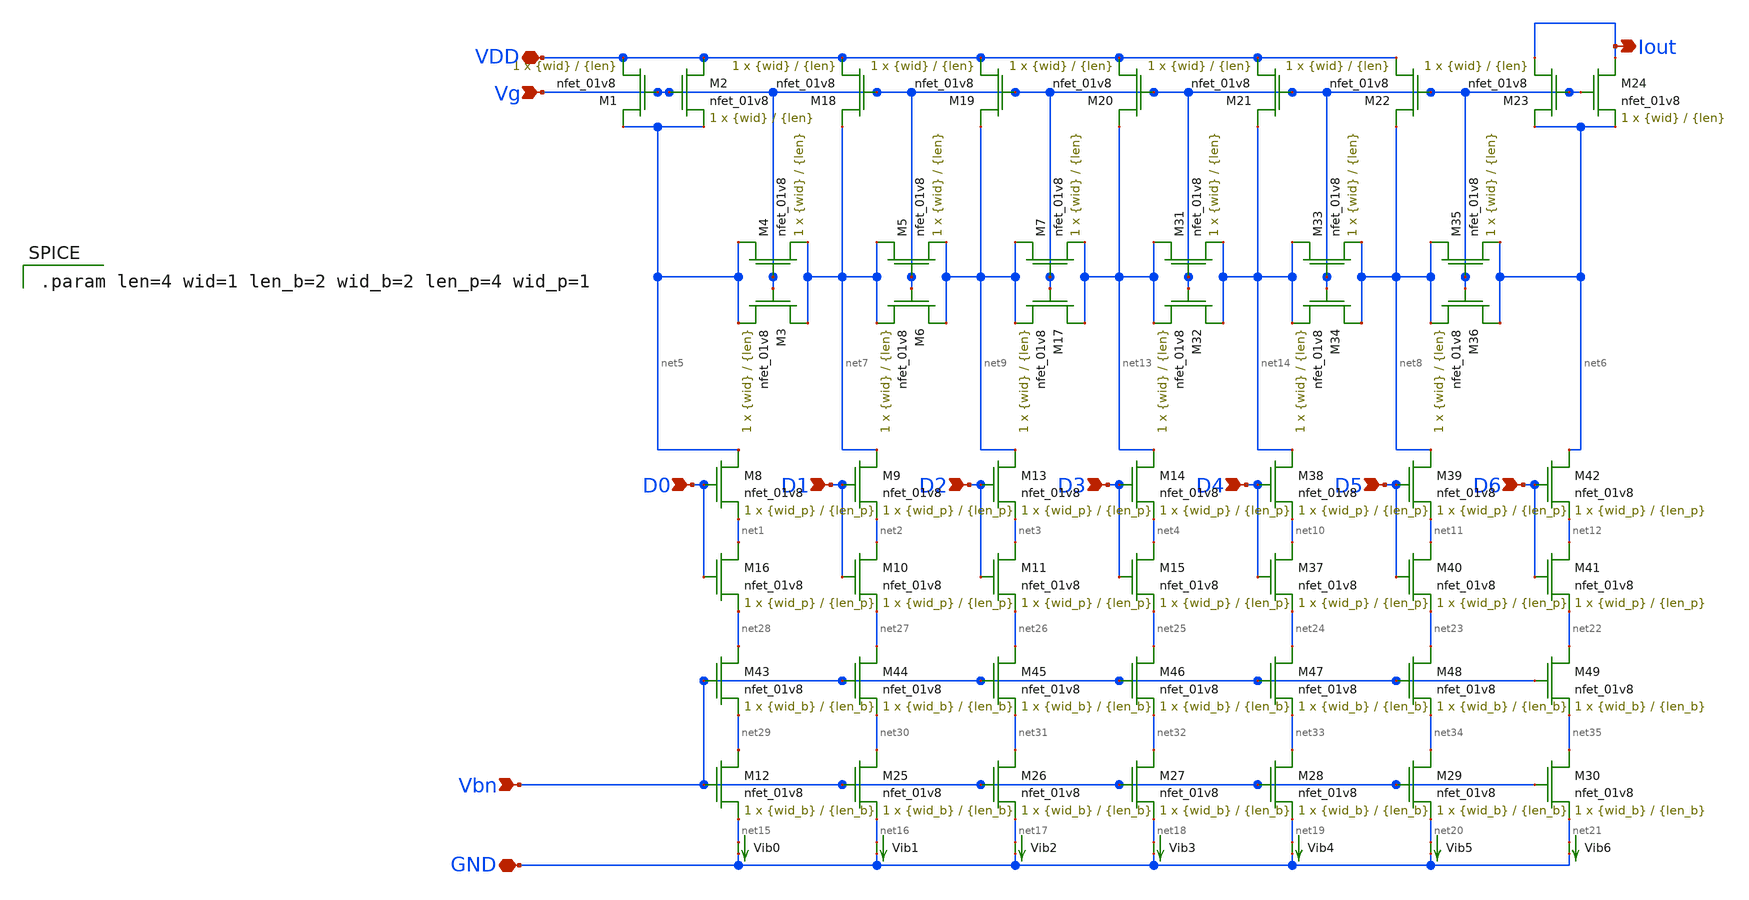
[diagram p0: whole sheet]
** sch_path: mp3/ladder.sch
**.subckt ladder Vbn VDD Iout GND D0 D1 D2 D3 D4 D5 D6 Vg
*.ipin Vbn
*.iopin VDD
*.opin Iout
*.iopin GND
*.ipin D0
*.ipin D1
*.ipin D2
*.ipin D3
*.ipin D4
*.ipin D5
*.ipin D6
*.ipin Vg
XM1 net5 Vg VDD GND sky130_fd_pr__nfet_01v8 L={len} W={wid} nf=1 ad='int((nf+1)/2) * W/nf * 0.29' as='int((nf+2)/2) * W/nf * 0.29'
+ pd='2*int((nf+1)/2) * (W/nf + 0.29)' ps='2*int((nf+2)/2) * (W/nf + 0.29)' nrd='0.29 / W' nrs='0.29 / W'
+ sa=0 sb=0 sd=0 mult=1 m=1
XM4 net5 Vg net7 GND sky130_fd_pr__nfet_01v8 L={len} W={wid} nf=1 ad='int((nf+1)/2) * W/nf * 0.29' as='int((nf+2)/2) * W/nf * 0.29'
+ pd='2*int((nf+1)/2) * (W/nf + 0.29)' ps='2*int((nf+2)/2) * (W/nf + 0.29)' nrd='0.29 / W' nrs='0.29 / W'
+ sa=0 sb=0 sd=0 mult=1 m=1
XM12 net29 Vbn net15 GND sky130_fd_pr__nfet_01v8 L={len_b} W={wid_b} nf=1 ad='int((nf+1)/2) * W/nf * 0.29'
+ as='int((nf+2)/2) * W/nf * 0.29' pd='2*int((nf+1)/2) * (W/nf + 0.29)' ps='2*int((nf+2)/2) * (W/nf + 0.29)'
+ nrd='0.29 / W' nrs='0.29 / W' sa=0 sb=0 sd=0 mult=1 m=1
XM2 VDD Vg net5 GND sky130_fd_pr__nfet_01v8 L={len} W={wid} nf=1 ad='int((nf+1)/2) * W/nf * 0.29' as='int((nf+2)/2) * W/nf * 0.29'
+ pd='2*int((nf+1)/2) * (W/nf + 0.29)' ps='2*int((nf+2)/2) * (W/nf + 0.29)' nrd='0.29 / W' nrs='0.29 / W'
+ sa=0 sb=0 sd=0 mult=1 m=1
XM18 net7 Vg VDD GND sky130_fd_pr__nfet_01v8 L={len} W={wid} nf=1 ad='int((nf+1)/2) * W/nf * 0.29' as='int((nf+2)/2) * W/nf * 0.29'
+ pd='2*int((nf+1)/2) * (W/nf + 0.29)' ps='2*int((nf+2)/2) * (W/nf + 0.29)' nrd='0.29 / W' nrs='0.29 / W'
+ sa=0 sb=0 sd=0 mult=1 m=1
XM19 net9 Vg VDD GND sky130_fd_pr__nfet_01v8 L={len} W={wid} nf=1 ad='int((nf+1)/2) * W/nf * 0.29' as='int((nf+2)/2) * W/nf * 0.29'
+ pd='2*int((nf+1)/2) * (W/nf + 0.29)' ps='2*int((nf+2)/2) * (W/nf + 0.29)' nrd='0.29 / W' nrs='0.29 / W'
+ sa=0 sb=0 sd=0 mult=1 m=1
XM20 net13 Vg VDD GND sky130_fd_pr__nfet_01v8 L={len} W={wid} nf=1 ad='int((nf+1)/2) * W/nf * 0.29' as='int((nf+2)/2) * W/nf * 0.29'
+ pd='2*int((nf+1)/2) * (W/nf + 0.29)' ps='2*int((nf+2)/2) * (W/nf + 0.29)' nrd='0.29 / W' nrs='0.29 / W'
+ sa=0 sb=0 sd=0 mult=1 m=1
XM21 net14 Vg VDD GND sky130_fd_pr__nfet_01v8 L={len} W={wid} nf=1 ad='int((nf+1)/2) * W/nf * 0.29' as='int((nf+2)/2) * W/nf * 0.29'
+ pd='2*int((nf+1)/2) * (W/nf + 0.29)' ps='2*int((nf+2)/2) * (W/nf + 0.29)' nrd='0.29 / W' nrs='0.29 / W'
+ sa=0 sb=0 sd=0 mult=1 m=1
XM22 net8 Vg VDD GND sky130_fd_pr__nfet_01v8 L={len} W={wid} nf=1 ad='int((nf+1)/2) * W/nf * 0.29' as='int((nf+2)/2) * W/nf * 0.29'
+ pd='2*int((nf+1)/2) * (W/nf + 0.29)' ps='2*int((nf+2)/2) * (W/nf + 0.29)' nrd='0.29 / W' nrs='0.29 / W'
+ sa=0 sb=0 sd=0 mult=1 m=1
XM23 net6 Vg Iout GND sky130_fd_pr__nfet_01v8 L={len} W={wid} nf=1 ad='int((nf+1)/2) * W/nf * 0.29' as='int((nf+2)/2) * W/nf * 0.29'
+ pd='2*int((nf+1)/2) * (W/nf + 0.29)' ps='2*int((nf+2)/2) * (W/nf + 0.29)' nrd='0.29 / W' nrs='0.29 / W'
+ sa=0 sb=0 sd=0 mult=1 m=1
XM24 Iout Vg net6 GND sky130_fd_pr__nfet_01v8 L={len} W={wid} nf=1 ad='int((nf+1)/2) * W/nf * 0.29' as='int((nf+2)/2) * W/nf * 0.29'
+ pd='2*int((nf+1)/2) * (W/nf + 0.29)' ps='2*int((nf+2)/2) * (W/nf + 0.29)' nrd='0.29 / W' nrs='0.29 / W'
+ sa=0 sb=0 sd=0 mult=1 m=1
XM3 net7 Vg net5 GND sky130_fd_pr__nfet_01v8 L={len} W={wid} nf=1 ad='int((nf+1)/2) * W/nf * 0.29' as='int((nf+2)/2) * W/nf * 0.29'
+ pd='2*int((nf+1)/2) * (W/nf + 0.29)' ps='2*int((nf+2)/2) * (W/nf + 0.29)' nrd='0.29 / W' nrs='0.29 / W'
+ sa=0 sb=0 sd=0 mult=1 m=1
XM5 net7 Vg net9 GND sky130_fd_pr__nfet_01v8 L={len} W={wid} nf=1 ad='int((nf+1)/2) * W/nf * 0.29' as='int((nf+2)/2) * W/nf * 0.29'
+ pd='2*int((nf+1)/2) * (W/nf + 0.29)' ps='2*int((nf+2)/2) * (W/nf + 0.29)' nrd='0.29 / W' nrs='0.29 / W'
+ sa=0 sb=0 sd=0 mult=1 m=1
XM6 net9 Vg net7 GND sky130_fd_pr__nfet_01v8 L={len} W={wid} nf=1 ad='int((nf+1)/2) * W/nf * 0.29' as='int((nf+2)/2) * W/nf * 0.29'
+ pd='2*int((nf+1)/2) * (W/nf + 0.29)' ps='2*int((nf+2)/2) * (W/nf + 0.29)' nrd='0.29 / W' nrs='0.29 / W'
+ sa=0 sb=0 sd=0 mult=1 m=1
XM7 net9 Vg net13 GND sky130_fd_pr__nfet_01v8 L={len} W={wid} nf=1 ad='int((nf+1)/2) * W/nf * 0.29' as='int((nf+2)/2) * W/nf * 0.29'
+ pd='2*int((nf+1)/2) * (W/nf + 0.29)' ps='2*int((nf+2)/2) * (W/nf + 0.29)' nrd='0.29 / W' nrs='0.29 / W'
+ sa=0 sb=0 sd=0 mult=1 m=1
XM17 net13 Vg net9 GND sky130_fd_pr__nfet_01v8 L={len} W={wid} nf=1 ad='int((nf+1)/2) * W/nf * 0.29'
+ as='int((nf+2)/2) * W/nf * 0.29' pd='2*int((nf+1)/2) * (W/nf + 0.29)' ps='2*int((nf+2)/2) * (W/nf + 0.29)'
+ nrd='0.29 / W' nrs='0.29 / W' sa=0 sb=0 sd=0 mult=1 m=1
XM31 net13 Vg net14 GND sky130_fd_pr__nfet_01v8 L={len} W={wid} nf=1 ad='int((nf+1)/2) * W/nf * 0.29'
+ as='int((nf+2)/2) * W/nf * 0.29' pd='2*int((nf+1)/2) * (W/nf + 0.29)' ps='2*int((nf+2)/2) * (W/nf + 0.29)'
+ nrd='0.29 / W' nrs='0.29 / W' sa=0 sb=0 sd=0 mult=1 m=1
XM32 net14 Vg net13 GND sky130_fd_pr__nfet_01v8 L={len} W={wid} nf=1 ad='int((nf+1)/2) * W/nf * 0.29'
+ as='int((nf+2)/2) * W/nf * 0.29' pd='2*int((nf+1)/2) * (W/nf + 0.29)' ps='2*int((nf+2)/2) * (W/nf + 0.29)'
+ nrd='0.29 / W' nrs='0.29 / W' sa=0 sb=0 sd=0 mult=1 m=1
XM33 net14 Vg net8 GND sky130_fd_pr__nfet_01v8 L={len} W={wid} nf=1 ad='int((nf+1)/2) * W/nf * 0.29'
+ as='int((nf+2)/2) * W/nf * 0.29' pd='2*int((nf+1)/2) * (W/nf + 0.29)' ps='2*int((nf+2)/2) * (W/nf + 0.29)'
+ nrd='0.29 / W' nrs='0.29 / W' sa=0 sb=0 sd=0 mult=1 m=1
XM34 net8 Vg net14 GND sky130_fd_pr__nfet_01v8 L={len} W={wid} nf=1 ad='int((nf+1)/2) * W/nf * 0.29'
+ as='int((nf+2)/2) * W/nf * 0.29' pd='2*int((nf+1)/2) * (W/nf + 0.29)' ps='2*int((nf+2)/2) * (W/nf + 0.29)'
+ nrd='0.29 / W' nrs='0.29 / W' sa=0 sb=0 sd=0 mult=1 m=1
XM35 net8 Vg net6 GND sky130_fd_pr__nfet_01v8 L={len} W={wid} nf=1 ad='int((nf+1)/2) * W/nf * 0.29' as='int((nf+2)/2) * W/nf * 0.29'
+ pd='2*int((nf+1)/2) * (W/nf + 0.29)' ps='2*int((nf+2)/2) * (W/nf + 0.29)' nrd='0.29 / W' nrs='0.29 / W'
+ sa=0 sb=0 sd=0 mult=1 m=1
XM36 net6 Vg net8 GND sky130_fd_pr__nfet_01v8 L={len} W={wid} nf=1 ad='int((nf+1)/2) * W/nf * 0.29' as='int((nf+2)/2) * W/nf * 0.29'
+ pd='2*int((nf+1)/2) * (W/nf + 0.29)' ps='2*int((nf+2)/2) * (W/nf + 0.29)' nrd='0.29 / W' nrs='0.29 / W'
+ sa=0 sb=0 sd=0 mult=1 m=1
Vib0 net15 GND 0
.save i(vib0)
Vib1 net16 GND 0
.save i(vib1)
Vib2 net17 GND 0
.save i(vib2)
Vib3 net18 GND 0
.save i(vib3)
Vib4 net19 GND 0
.save i(vib4)
Vib5 net20 GND 0
.save i(vib5)
Vib6 net21 GND 0
.save i(vib6)
XM16 net1 D0 net28 GND sky130_fd_pr__nfet_01v8 L={len_p} W={wid_p} nf=1 ad='int((nf+1)/2) * W/nf * 0.29'
+ as='int((nf+2)/2) * W/nf * 0.29' pd='2*int((nf+1)/2) * (W/nf + 0.29)' ps='2*int((nf+2)/2) * (W/nf + 0.29)'
+ nrd='0.29 / W' nrs='0.29 / W' sa=0 sb=0 sd=0 mult=1 m=1
XM8 net5 D0 net1 GND sky130_fd_pr__nfet_01v8 L={len_p} W={wid_p} nf=1 ad='int((nf+1)/2) * W/nf * 0.29'
+ as='int((nf+2)/2) * W/nf * 0.29' pd='2*int((nf+1)/2) * (W/nf + 0.29)' ps='2*int((nf+2)/2) * (W/nf + 0.29)'
+ nrd='0.29 / W' nrs='0.29 / W' sa=0 sb=0 sd=0 mult=1 m=1
XM9 net7 D1 net2 GND sky130_fd_pr__nfet_01v8 L={len_p} W={wid_p} nf=1 ad='int((nf+1)/2) * W/nf * 0.29'
+ as='int((nf+2)/2) * W/nf * 0.29' pd='2*int((nf+1)/2) * (W/nf + 0.29)' ps='2*int((nf+2)/2) * (W/nf + 0.29)'
+ nrd='0.29 / W' nrs='0.29 / W' sa=0 sb=0 sd=0 mult=1 m=1
XM10 net2 D1 net27 GND sky130_fd_pr__nfet_01v8 L={len_p} W={wid_p} nf=1 ad='int((nf+1)/2) * W/nf * 0.29'
+ as='int((nf+2)/2) * W/nf * 0.29' pd='2*int((nf+1)/2) * (W/nf + 0.29)' ps='2*int((nf+2)/2) * (W/nf + 0.29)'
+ nrd='0.29 / W' nrs='0.29 / W' sa=0 sb=0 sd=0 mult=1 m=1
XM11 net3 D2 net26 GND sky130_fd_pr__nfet_01v8 L={len_p} W={wid_p} nf=1 ad='int((nf+1)/2) * W/nf * 0.29'
+ as='int((nf+2)/2) * W/nf * 0.29' pd='2*int((nf+1)/2) * (W/nf + 0.29)' ps='2*int((nf+2)/2) * (W/nf + 0.29)'
+ nrd='0.29 / W' nrs='0.29 / W' sa=0 sb=0 sd=0 mult=1 m=1
XM13 net9 D2 net3 GND sky130_fd_pr__nfet_01v8 L={len_p} W={wid_p} nf=1 ad='int((nf+1)/2) * W/nf * 0.29'
+ as='int((nf+2)/2) * W/nf * 0.29' pd='2*int((nf+1)/2) * (W/nf + 0.29)' ps='2*int((nf+2)/2) * (W/nf + 0.29)'
+ nrd='0.29 / W' nrs='0.29 / W' sa=0 sb=0 sd=0 mult=1 m=1
XM14 net13 D3 net4 GND sky130_fd_pr__nfet_01v8 L={len_p} W={wid_p} nf=1 ad='int((nf+1)/2) * W/nf * 0.29'
+ as='int((nf+2)/2) * W/nf * 0.29' pd='2*int((nf+1)/2) * (W/nf + 0.29)' ps='2*int((nf+2)/2) * (W/nf + 0.29)'
+ nrd='0.29 / W' nrs='0.29 / W' sa=0 sb=0 sd=0 mult=1 m=1
XM15 net4 D3 net25 GND sky130_fd_pr__nfet_01v8 L={len_p} W={wid_p} nf=1 ad='int((nf+1)/2) * W/nf * 0.29'
+ as='int((nf+2)/2) * W/nf * 0.29' pd='2*int((nf+1)/2) * (W/nf + 0.29)' ps='2*int((nf+2)/2) * (W/nf + 0.29)'
+ nrd='0.29 / W' nrs='0.29 / W' sa=0 sb=0 sd=0 mult=1 m=1
XM37 net10 D4 net24 GND sky130_fd_pr__nfet_01v8 L={len_p} W={wid_p} nf=1 ad='int((nf+1)/2) * W/nf * 0.29'
+ as='int((nf+2)/2) * W/nf * 0.29' pd='2*int((nf+1)/2) * (W/nf + 0.29)' ps='2*int((nf+2)/2) * (W/nf + 0.29)'
+ nrd='0.29 / W' nrs='0.29 / W' sa=0 sb=0 sd=0 mult=1 m=1
XM38 net14 D4 net10 GND sky130_fd_pr__nfet_01v8 L={len_p} W={wid_p} nf=1 ad='int((nf+1)/2) * W/nf * 0.29'
+ as='int((nf+2)/2) * W/nf * 0.29' pd='2*int((nf+1)/2) * (W/nf + 0.29)' ps='2*int((nf+2)/2) * (W/nf + 0.29)'
+ nrd='0.29 / W' nrs='0.29 / W' sa=0 sb=0 sd=0 mult=1 m=1
XM39 net8 D5 net11 GND sky130_fd_pr__nfet_01v8 L={len_p} W={wid_p} nf=1 ad='int((nf+1)/2) * W/nf * 0.29'
+ as='int((nf+2)/2) * W/nf * 0.29' pd='2*int((nf+1)/2) * (W/nf + 0.29)' ps='2*int((nf+2)/2) * (W/nf + 0.29)'
+ nrd='0.29 / W' nrs='0.29 / W' sa=0 sb=0 sd=0 mult=1 m=1
XM40 net11 D5 net23 GND sky130_fd_pr__nfet_01v8 L={len_p} W={wid_p} nf=1 ad='int((nf+1)/2) * W/nf * 0.29'
+ as='int((nf+2)/2) * W/nf * 0.29' pd='2*int((nf+1)/2) * (W/nf + 0.29)' ps='2*int((nf+2)/2) * (W/nf + 0.29)'
+ nrd='0.29 / W' nrs='0.29 / W' sa=0 sb=0 sd=0 mult=1 m=1
XM41 net12 D6 net22 GND sky130_fd_pr__nfet_01v8 L={len_p} W={wid_p} nf=1 ad='int((nf+1)/2) * W/nf * 0.29'
+ as='int((nf+2)/2) * W/nf * 0.29' pd='2*int((nf+1)/2) * (W/nf + 0.29)' ps='2*int((nf+2)/2) * (W/nf + 0.29)'
+ nrd='0.29 / W' nrs='0.29 / W' sa=0 sb=0 sd=0 mult=1 m=1
XM42 net6 D6 net12 GND sky130_fd_pr__nfet_01v8 L={len_p} W={wid_p} nf=1 ad='int((nf+1)/2) * W/nf * 0.29'
+ as='int((nf+2)/2) * W/nf * 0.29' pd='2*int((nf+1)/2) * (W/nf + 0.29)' ps='2*int((nf+2)/2) * (W/nf + 0.29)'
+ nrd='0.29 / W' nrs='0.29 / W' sa=0 sb=0 sd=0 mult=1 m=1
XM25 net30 Vbn net16 GND sky130_fd_pr__nfet_01v8 L={len_b} W={wid_b} nf=1 ad='int((nf+1)/2) * W/nf * 0.29'
+ as='int((nf+2)/2) * W/nf * 0.29' pd='2*int((nf+1)/2) * (W/nf + 0.29)' ps='2*int((nf+2)/2) * (W/nf + 0.29)'
+ nrd='0.29 / W' nrs='0.29 / W' sa=0 sb=0 sd=0 mult=1 m=1
XM26 net31 Vbn net17 GND sky130_fd_pr__nfet_01v8 L={len_b} W={wid_b} nf=1 ad='int((nf+1)/2) * W/nf * 0.29'
+ as='int((nf+2)/2) * W/nf * 0.29' pd='2*int((nf+1)/2) * (W/nf + 0.29)' ps='2*int((nf+2)/2) * (W/nf + 0.29)'
+ nrd='0.29 / W' nrs='0.29 / W' sa=0 sb=0 sd=0 mult=1 m=1
XM27 net32 Vbn net18 GND sky130_fd_pr__nfet_01v8 L={len_b} W={wid_b} nf=1 ad='int((nf+1)/2) * W/nf * 0.29'
+ as='int((nf+2)/2) * W/nf * 0.29' pd='2*int((nf+1)/2) * (W/nf + 0.29)' ps='2*int((nf+2)/2) * (W/nf + 0.29)'
+ nrd='0.29 / W' nrs='0.29 / W' sa=0 sb=0 sd=0 mult=1 m=1
XM28 net33 Vbn net19 GND sky130_fd_pr__nfet_01v8 L={len_b} W={wid_b} nf=1 ad='int((nf+1)/2) * W/nf * 0.29'
+ as='int((nf+2)/2) * W/nf * 0.29' pd='2*int((nf+1)/2) * (W/nf + 0.29)' ps='2*int((nf+2)/2) * (W/nf + 0.29)'
+ nrd='0.29 / W' nrs='0.29 / W' sa=0 sb=0 sd=0 mult=1 m=1
XM29 net34 Vbn net20 GND sky130_fd_pr__nfet_01v8 L={len_b} W={wid_b} nf=1 ad='int((nf+1)/2) * W/nf * 0.29'
+ as='int((nf+2)/2) * W/nf * 0.29' pd='2*int((nf+1)/2) * (W/nf + 0.29)' ps='2*int((nf+2)/2) * (W/nf + 0.29)'
+ nrd='0.29 / W' nrs='0.29 / W' sa=0 sb=0 sd=0 mult=1 m=1
XM30 net35 Vbn net21 GND sky130_fd_pr__nfet_01v8 L={len_b} W={wid_b} nf=1 ad='int((nf+1)/2) * W/nf * 0.29'
+ as='int((nf+2)/2) * W/nf * 0.29' pd='2*int((nf+1)/2) * (W/nf + 0.29)' ps='2*int((nf+2)/2) * (W/nf + 0.29)'
+ nrd='0.29 / W' nrs='0.29 / W' sa=0 sb=0 sd=0 mult=1 m=1
XM43 net28 Vbn net29 GND sky130_fd_pr__nfet_01v8 L={len_b} W={wid_b} nf=1 ad='int((nf+1)/2) * W/nf * 0.29'
+ as='int((nf+2)/2) * W/nf * 0.29' pd='2*int((nf+1)/2) * (W/nf + 0.29)' ps='2*int((nf+2)/2) * (W/nf + 0.29)'
+ nrd='0.29 / W' nrs='0.29 / W' sa=0 sb=0 sd=0 mult=1 m=1
XM44 net27 Vbn net30 GND sky130_fd_pr__nfet_01v8 L={len_b} W={wid_b} nf=1 ad='int((nf+1)/2) * W/nf * 0.29'
+ as='int((nf+2)/2) * W/nf * 0.29' pd='2*int((nf+1)/2) * (W/nf + 0.29)' ps='2*int((nf+2)/2) * (W/nf + 0.29)'
+ nrd='0.29 / W' nrs='0.29 / W' sa=0 sb=0 sd=0 mult=1 m=1
XM45 net26 Vbn net31 GND sky130_fd_pr__nfet_01v8 L={len_b} W={wid_b} nf=1 ad='int((nf+1)/2) * W/nf * 0.29'
+ as='int((nf+2)/2) * W/nf * 0.29' pd='2*int((nf+1)/2) * (W/nf + 0.29)' ps='2*int((nf+2)/2) * (W/nf + 0.29)'
+ nrd='0.29 / W' nrs='0.29 / W' sa=0 sb=0 sd=0 mult=1 m=1
XM46 net25 Vbn net32 GND sky130_fd_pr__nfet_01v8 L={len_b} W={wid_b} nf=1 ad='int((nf+1)/2) * W/nf * 0.29'
+ as='int((nf+2)/2) * W/nf * 0.29' pd='2*int((nf+1)/2) * (W/nf + 0.29)' ps='2*int((nf+2)/2) * (W/nf + 0.29)'
+ nrd='0.29 / W' nrs='0.29 / W' sa=0 sb=0 sd=0 mult=1 m=1
XM47 net24 Vbn net33 GND sky130_fd_pr__nfet_01v8 L={len_b} W={wid_b} nf=1 ad='int((nf+1)/2) * W/nf * 0.29'
+ as='int((nf+2)/2) * W/nf * 0.29' pd='2*int((nf+1)/2) * (W/nf + 0.29)' ps='2*int((nf+2)/2) * (W/nf + 0.29)'
+ nrd='0.29 / W' nrs='0.29 / W' sa=0 sb=0 sd=0 mult=1 m=1
XM48 net23 Vbn net34 GND sky130_fd_pr__nfet_01v8 L={len_b} W={wid_b} nf=1 ad='int((nf+1)/2) * W/nf * 0.29'
+ as='int((nf+2)/2) * W/nf * 0.29' pd='2*int((nf+1)/2) * (W/nf + 0.29)' ps='2*int((nf+2)/2) * (W/nf + 0.29)'
+ nrd='0.29 / W' nrs='0.29 / W' sa=0 sb=0 sd=0 mult=1 m=1
XM49 net22 Vbn net35 GND sky130_fd_pr__nfet_01v8 L={len_b} W={wid_b} nf=1 ad='int((nf+1)/2) * W/nf * 0.29'
+ as='int((nf+2)/2) * W/nf * 0.29' pd='2*int((nf+1)/2) * (W/nf + 0.29)' ps='2*int((nf+2)/2) * (W/nf + 0.29)'
+ nrd='0.29 / W' nrs='0.29 / W' sa=0 sb=0 sd=0 mult=1 m=1
**** begin user architecture code

.param len=4 wid=1 len_b=2 wid_b=2 len_p=4 wid_p=1

**** end user architecture code
**.ends
.end
